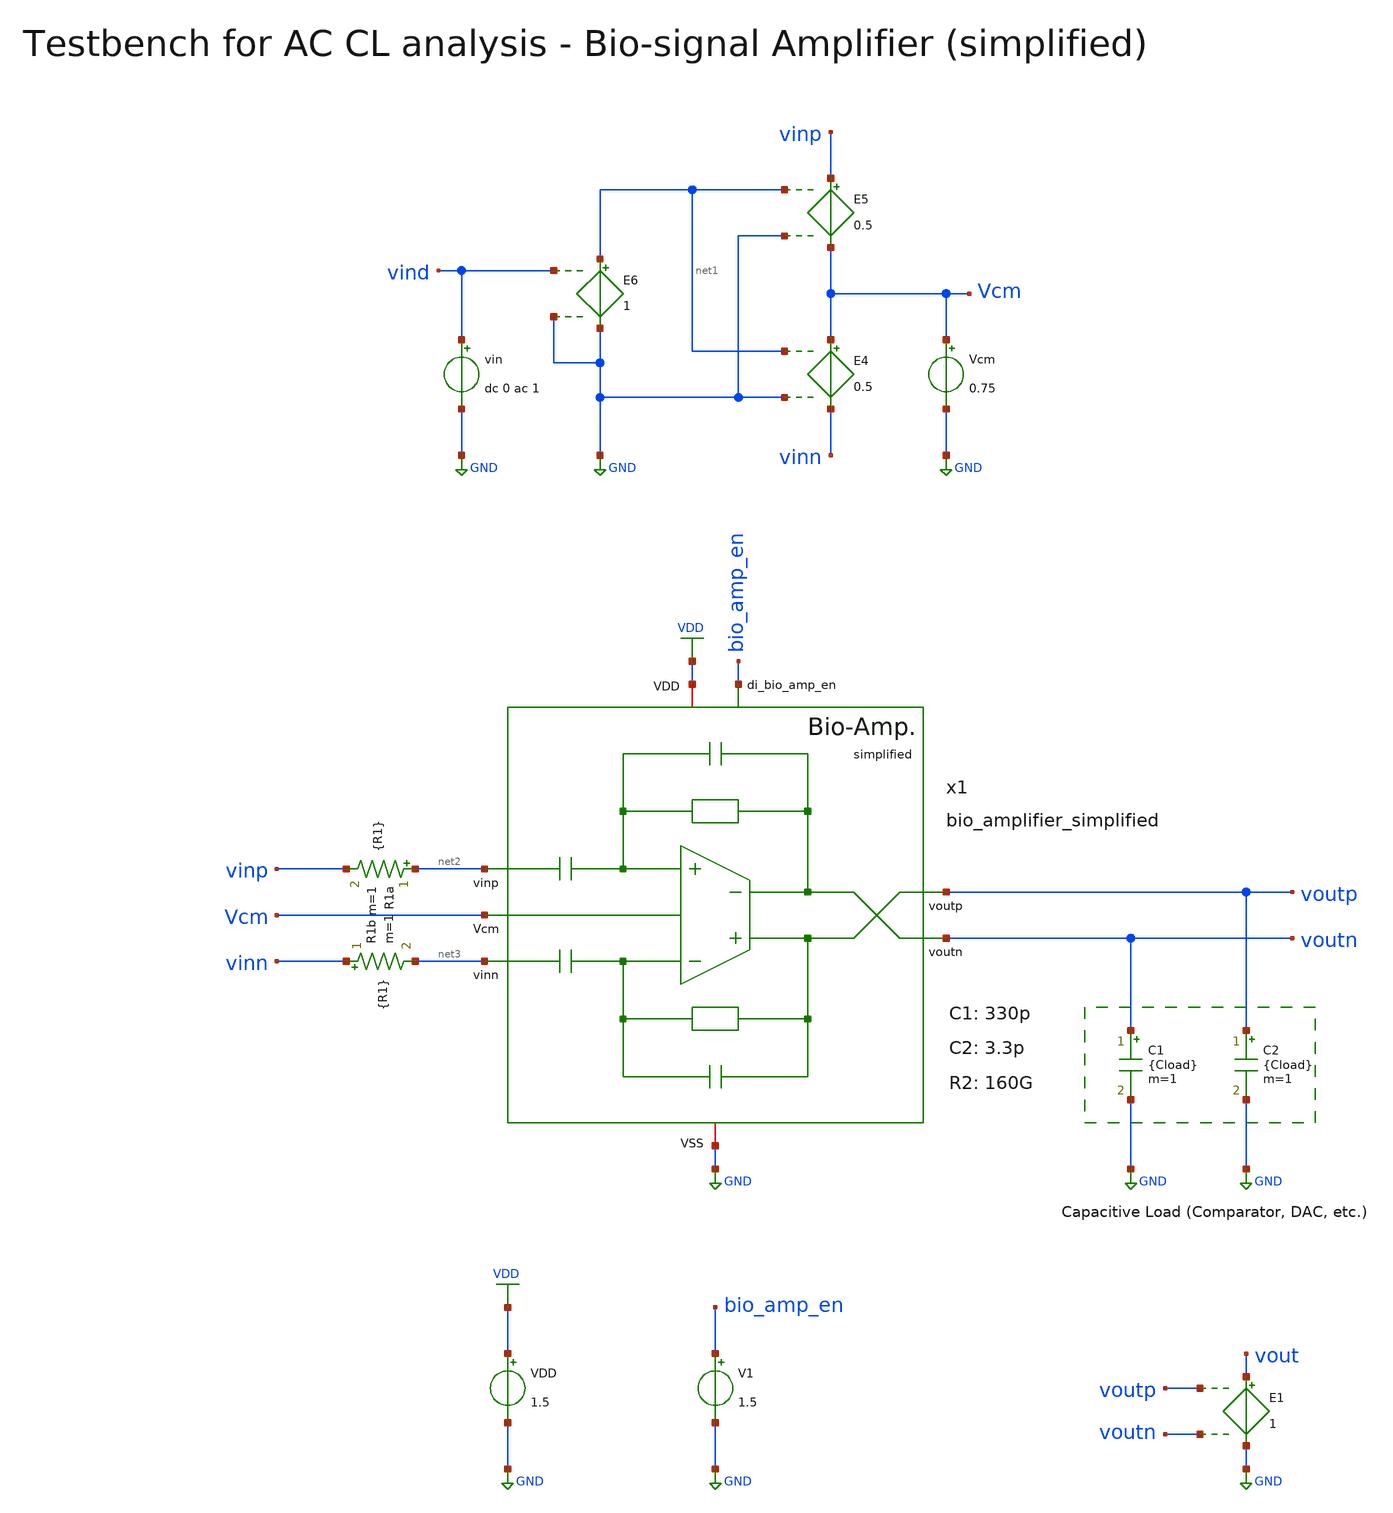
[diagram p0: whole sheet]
** sch_path: SG13G2_ATBS-ADC-main/xschem/bio_amplifier/testbenches/bio_amplifier_simplified_tb_ac_cl.sch
**.subckt bio_amplifier_simplified_tb_ac_cl
VDD VDD GND 1.5
C1 voutn GND {Cload} m=1
C2 voutp GND {Cload} m=1
Vcm Vcm GND 0.75
E4 Vcm vinn net1 GND 0.5
E5 vinp Vcm net1 GND 0.5
E6 net1 GND vind GND 1
V1 bio_amp_en GND 1.5
E1 vout GND voutp voutn 1
vin vind GND dc 0 ac 1
x1 voutp bio_amp_en net2 Vcm voutn net3 VDD GND bio_amplifier_simplified C1=330p C2=3.3p R2=160G
R1a net2 vinp {R1} m=1
R1b vinn net3 {R1} m=1
**** begin user architecture code

.lib cornerMOSlv.lib mos_tt
.lib cornerMOShv.lib mos_tt
.lib cornerRES.lib res_typ



.param temp=27
* 227.56fF DAC
.param Cload=227.56f
.param R1=1e-3
* 10Hz, C1 = 330p
*.param R1=48e6
* 10Hz, C1 = 165p
*.param R1=96e6
* 10Hz, C1 = 33p
*.param R1=480e6
* 500Hz
*.param R1=1e6
.options savecurrents method=gear reltol=1e-2 abstol=1e-15 gmin=1e-15 rshunt=1e12
.control

optran 0 0 0 1u 1m 0

save all
* save v(voutp) v(voutn) v(vout) v(vind)

set wr_vecnames
set wr_singlescale

* User Constants
let f_min = 0.01
let f_max = 1G
let fdc = 1

* Operating Point Analysis
op
remzerovec
write bio_amplifier_simplified_tb_ac_cl.raw
set appendwrite

* AC Analysis
ac dec 101 $&const.f_min $&const.f_max
remzerovec
write bio_amplifier_simplified_tb_ac_cl.raw
set appendwrite

* Plotting
let Amag = v(vout)/v(vind)
let Amag_dB = vdb(Amag)
let Aarg = 180/PI*cphase(Amag)

plot Amag_dB ylabel 'Magnitude'
plot Aarg ylabel 'Phase'
plot Amag_dB Aarg ylabel 'Magnitude, Phase'

* Measurements
meas ac Adc_cl_dB find Amag_dB when frequency = fdc
print Adc_cl_dB

let Amag_fc = Adc_cl_dB-3
meas ac fcl find frequency when Amag_dB = Amag_fc RISE=1
print fcl

meas ac fcu find frequency when Amag_dB = Amag_fc FALL=1
print fcu

* Write Data
set wr_vecnames
set wr_singlescale
wrdata
+ /foss/designs/SG13G2_ATBS-ADC-main/python/plot_simulations/data/bio_amplifier_simplified_tb_ac_cl.txt v(Amag_dB) v(Aarg)

*quit
.endc


**** end user architecture code
**.ends
.GLOBAL GND
.GLOBAL VDD
.end
